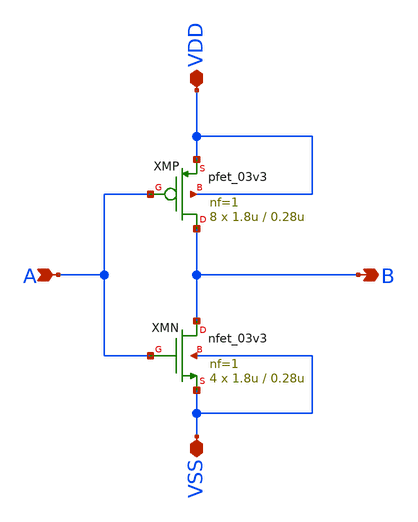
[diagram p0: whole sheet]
** sch_path: designs/DS_modulator/clkgen_inv/xscheme/clkgen_inv.sch
**.subckt clkgen_inv B A VDD VSS
*.opin B
*.ipin A
*.iopin VDD
*.iopin VSS
XMN B A VSS VSS nfet_03v3 L=0.28u W=1.8u nf=1 ad='int((nf+1)/2) * W/nf * 0.18u' as='int((nf+2)/2) * W/nf * 0.18u'
+ pd='2*int((nf+1)/2) * (W/nf + 0.18u)' ps='2*int((nf+2)/2) * (W/nf + 0.18u)' nrd='0.18u / W' nrs='0.18u / W'
+ sa=0 sb=0 sd=0 m=4
XMP B A VDD VDD pfet_03v3 L=0.28u W=1.8u nf=1 ad='int((nf+1)/2) * W/nf * 0.18u' as='int((nf+2)/2) * W/nf * 0.18u'
+ pd='2*int((nf+1)/2) * (W/nf + 0.18u)' ps='2*int((nf+2)/2) * (W/nf + 0.18u)' nrd='0.18u / W' nrs='0.18u / W'
+ sa=0 sb=0 sd=0 m=8
**.ends
.end
